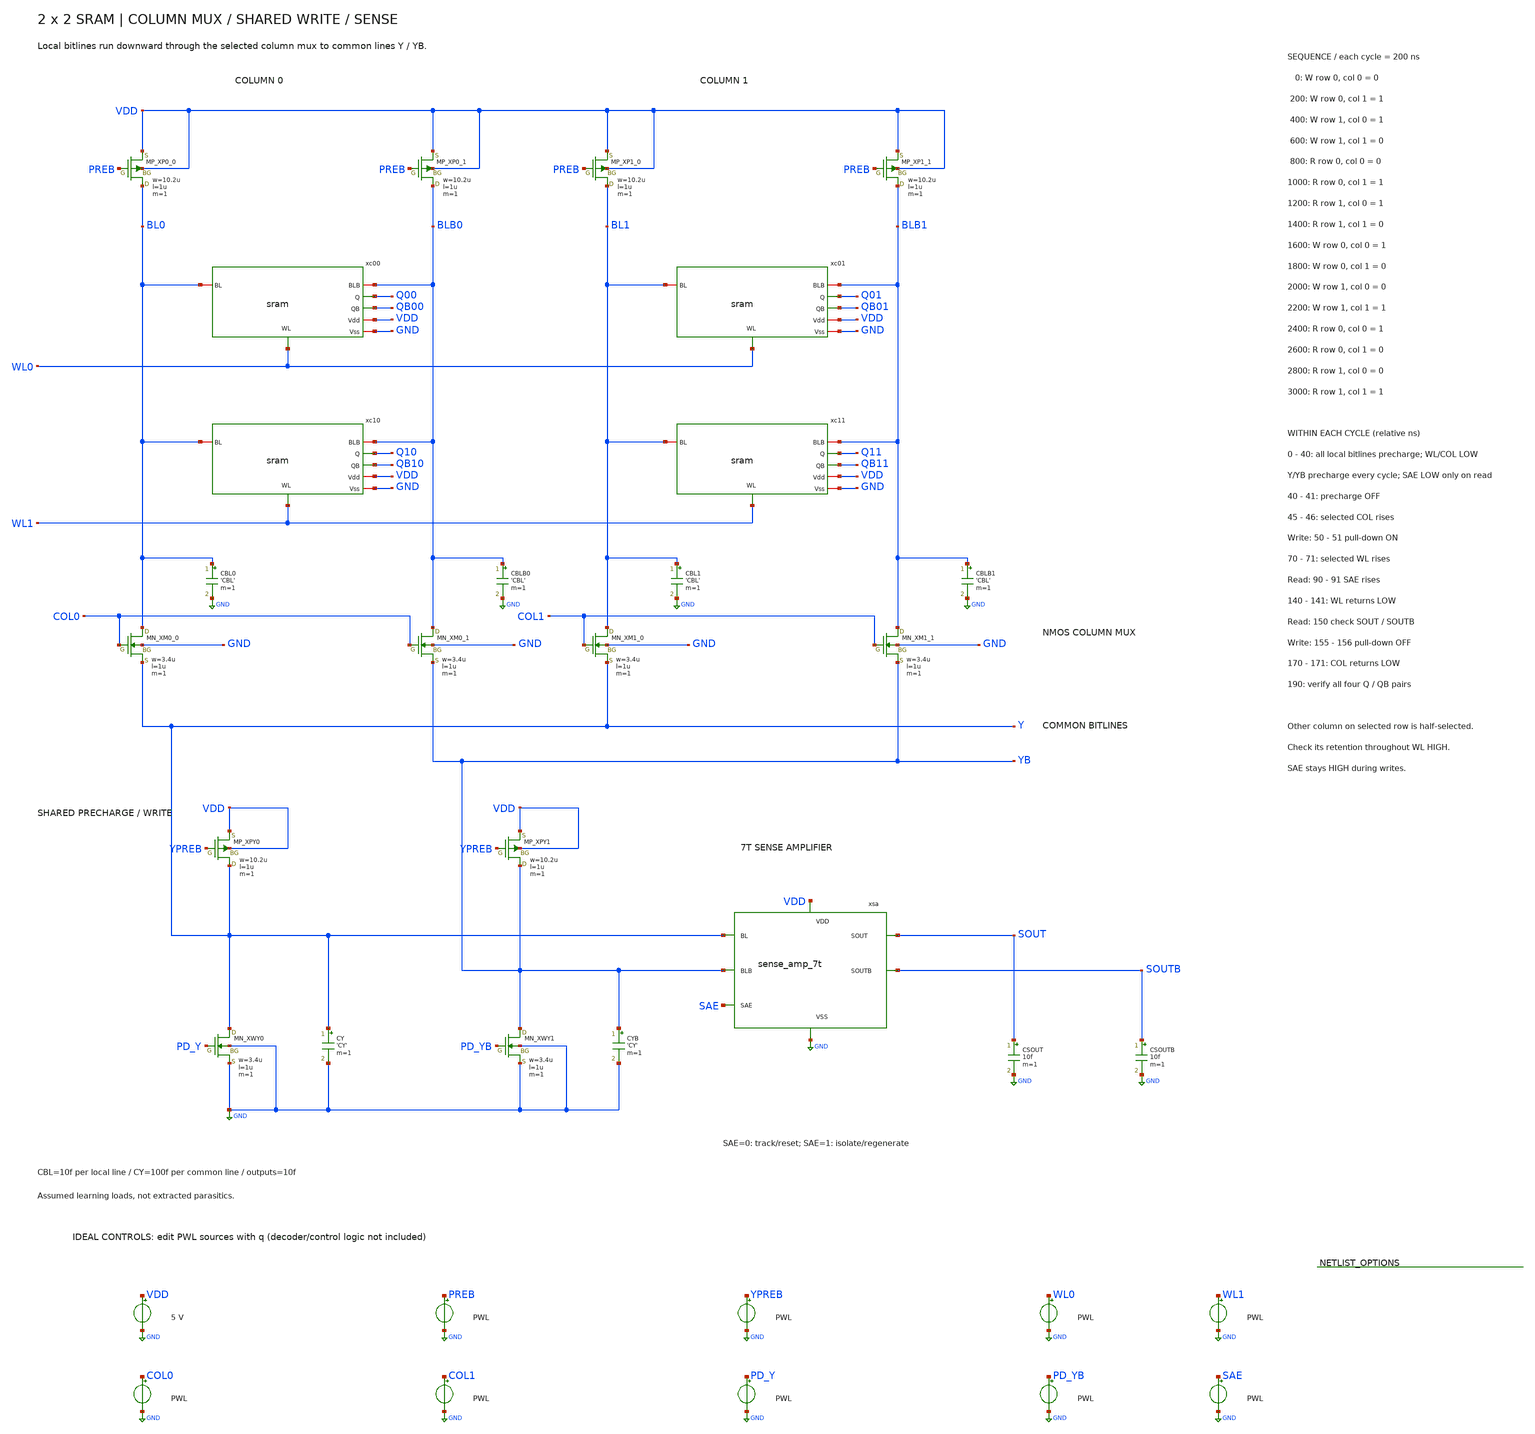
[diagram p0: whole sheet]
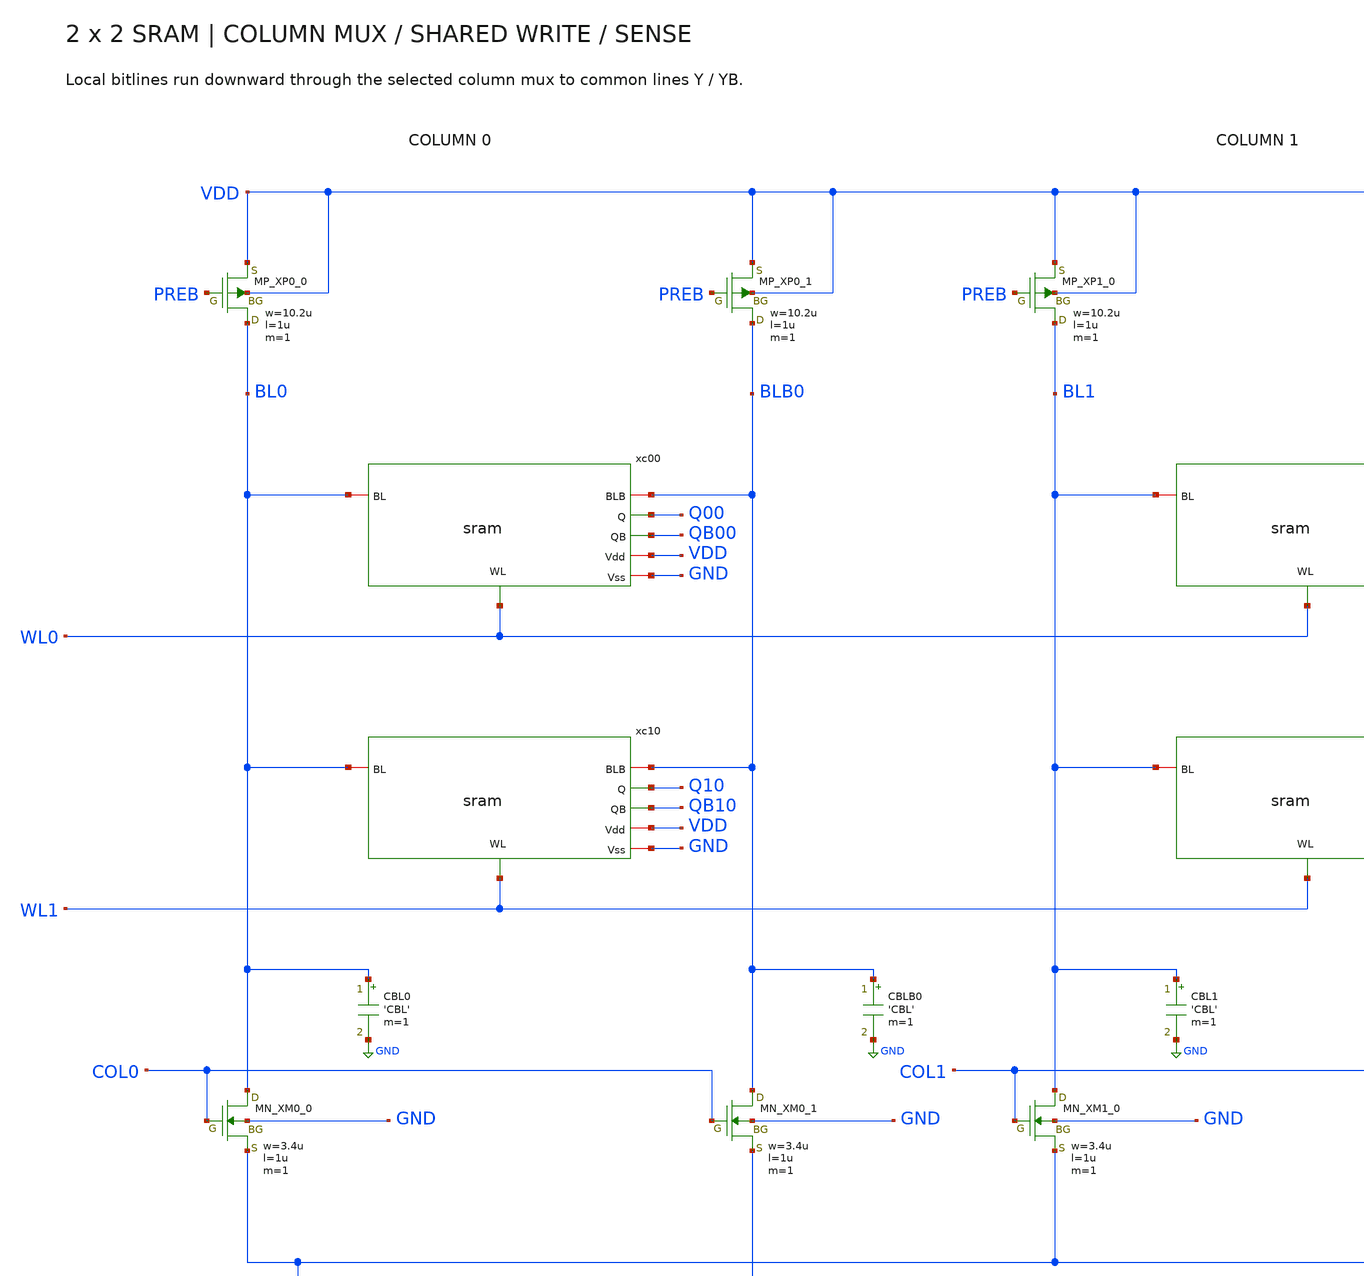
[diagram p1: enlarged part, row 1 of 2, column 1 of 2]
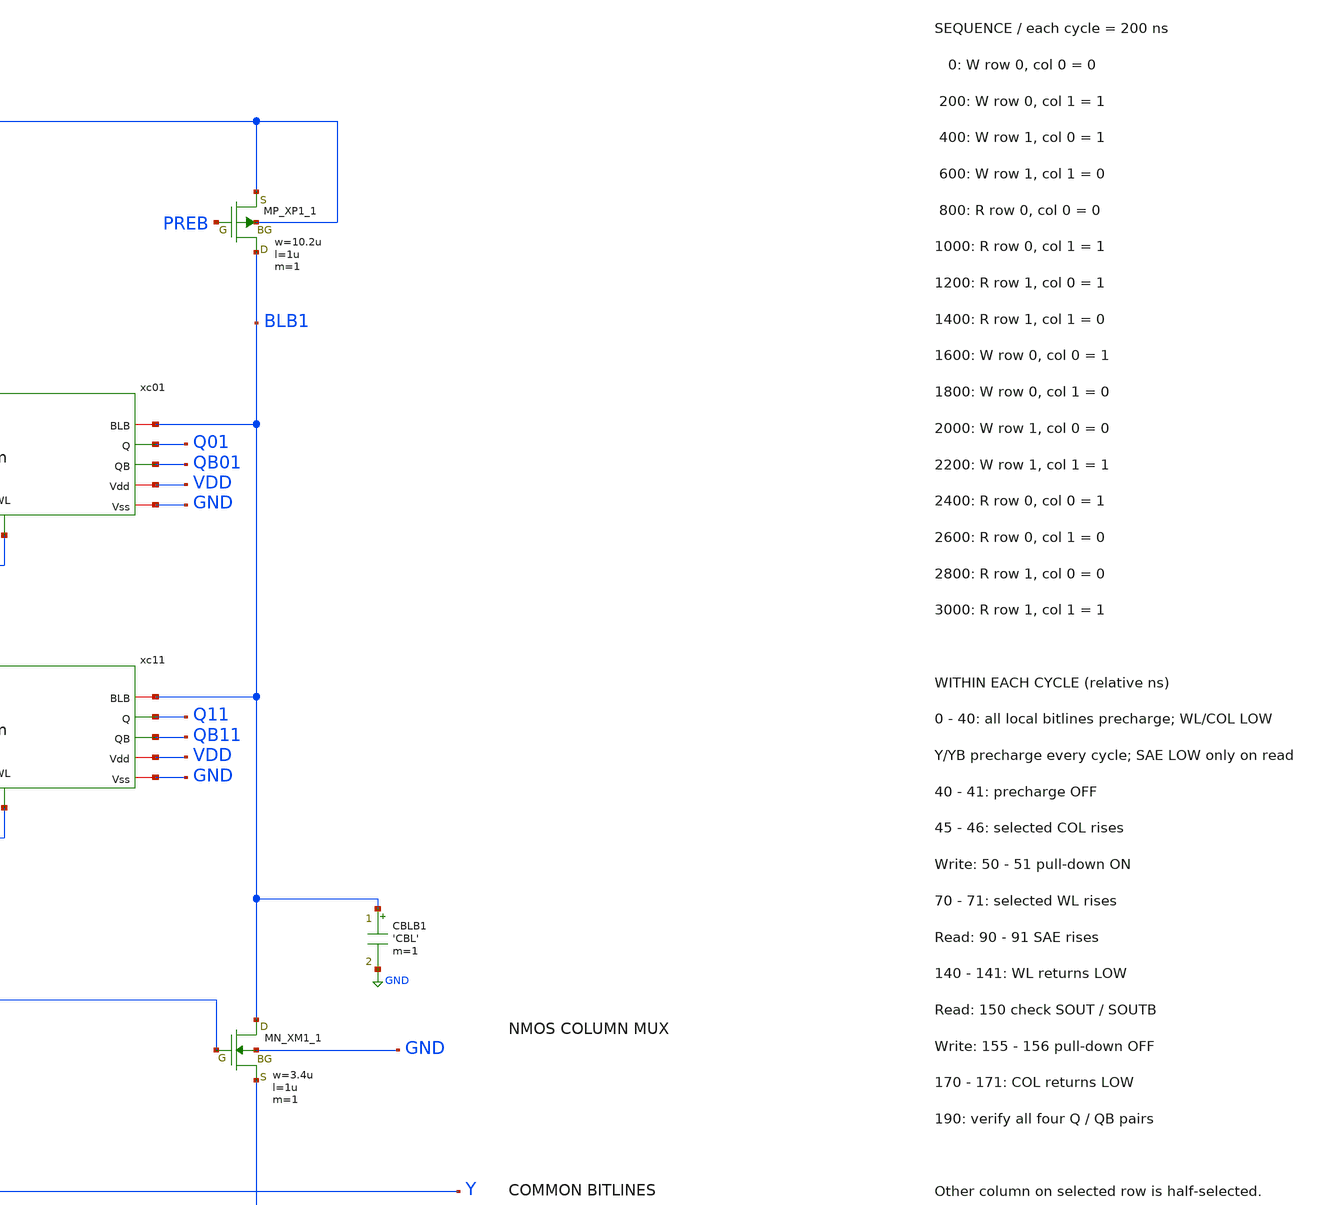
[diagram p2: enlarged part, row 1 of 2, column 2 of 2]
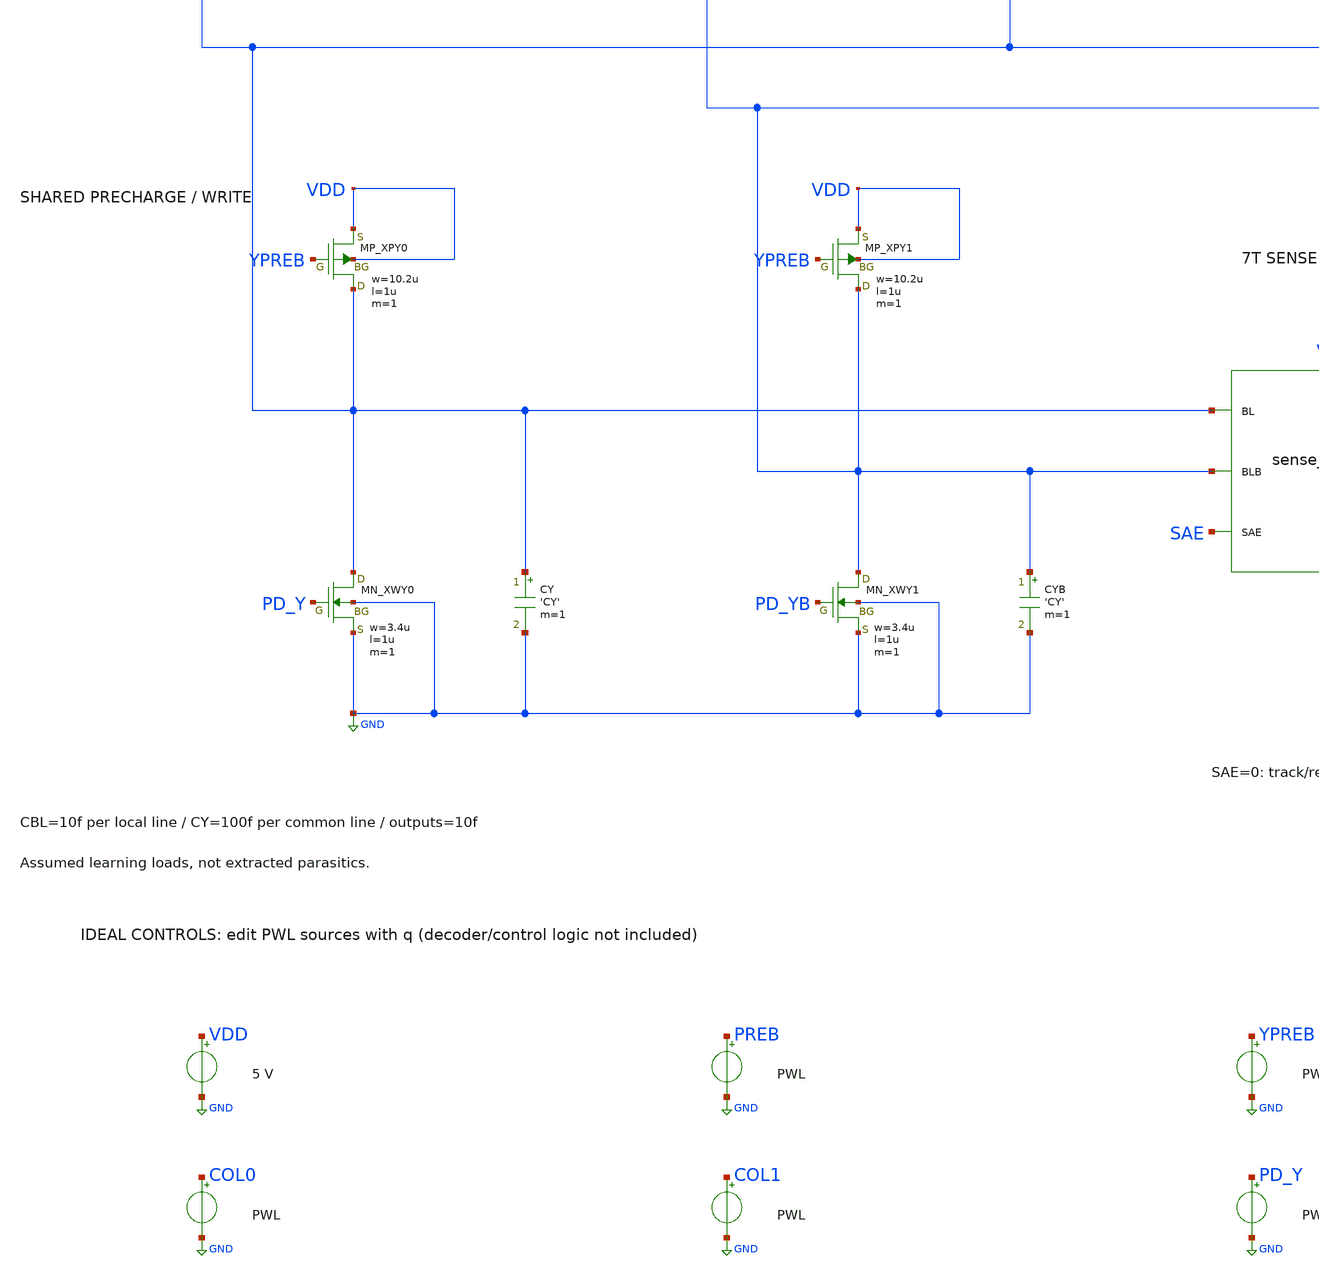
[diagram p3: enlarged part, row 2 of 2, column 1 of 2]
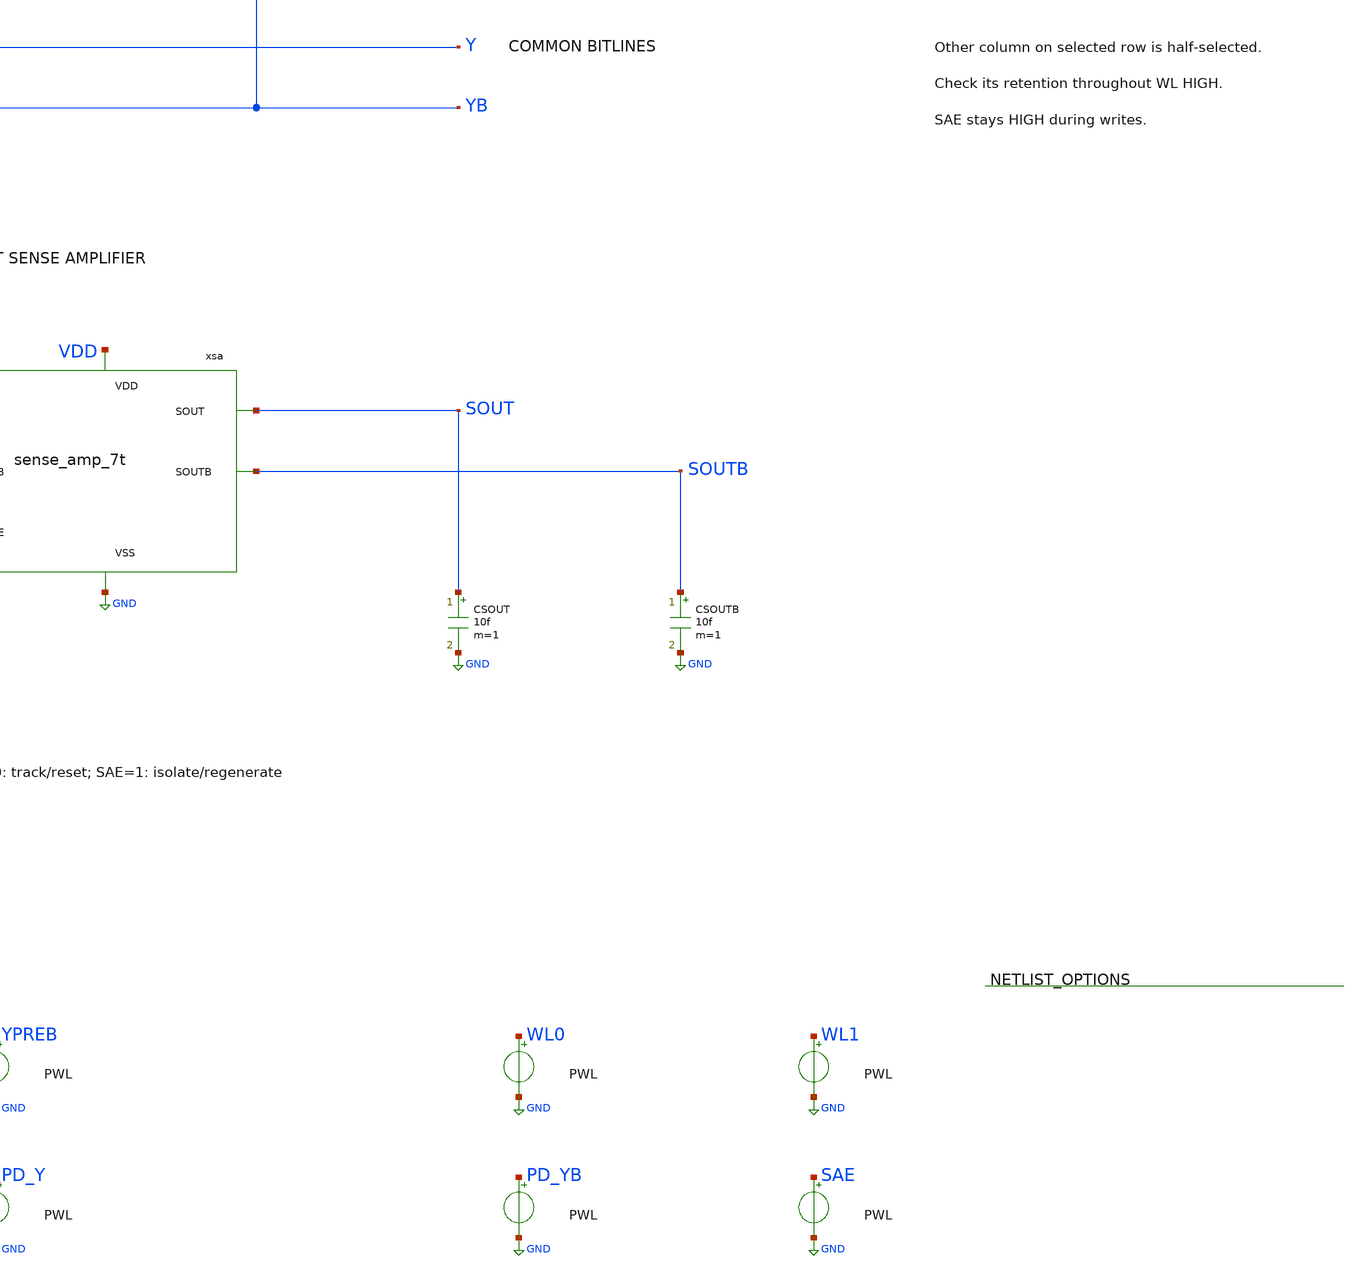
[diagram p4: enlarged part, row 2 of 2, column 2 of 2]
** sch_path: member_project/SRAM/PenguinEino/learning/schematics/sram_tb_array_mux.sch
**.subckt sram_tb_array_mux
XXP0_0 BL0 PREB VDD VDD PMOS w=10.2u l=1u nrd=0 nrs=0 m=1
CBL0 BL0 GND 'CBL' m=1
XXM0_0 BL0 COL0 Y GND NMOS w=3.4u l=1u nrd=0 nrs=0 m=1
XXP0_1 BLB0 PREB VDD VDD PMOS w=10.2u l=1u nrd=0 nrs=0 m=1
CBLB0 BLB0 GND 'CBL' m=1
XXM0_1 BLB0 COL0 YB GND NMOS w=3.4u l=1u nrd=0 nrs=0 m=1
xc00 WL0 VDD BLB0 Q00 QB00 BL0 GND sram
xc10 WL1 VDD BLB0 Q10 QB10 BL0 GND sram
XXP1_0 BL1 PREB VDD VDD PMOS w=10.2u l=1u nrd=0 nrs=0 m=1
CBL1 BL1 GND 'CBL' m=1
XXM1_0 BL1 COL1 Y GND NMOS w=3.4u l=1u nrd=0 nrs=0 m=1
XXP1_1 BLB1 PREB VDD VDD PMOS w=10.2u l=1u nrd=0 nrs=0 m=1
CBLB1 BLB1 GND 'CBL' m=1
XXM1_1 BLB1 COL1 YB GND NMOS w=3.4u l=1u nrd=0 nrs=0 m=1
xc01 WL0 VDD BLB1 Q01 QB01 BL1 GND sram
xc11 WL1 VDD BLB1 Q11 QB11 BL1 GND sram
XXPY0 Y YPREB VDD VDD PMOS w=10.2u l=1u nrd=0 nrs=0 m=1
XXWY0 Y PD_Y GND GND NMOS w=3.4u l=1u nrd=0 nrs=0 m=1
CY Y GND 'CY' m=1
XXPY1 YB YPREB VDD VDD PMOS w=10.2u l=1u nrd=0 nrs=0 m=1
XXWY1 YB PD_YB GND GND NMOS w=3.4u l=1u nrd=0 nrs=0 m=1
CYB YB GND 'CY' m=1
xsa Y YB SAE SOUT SOUTB VDD GND sense_amp_7t
CSOUT SOUT GND 10f m=1
CSOUTB SOUTB GND 10f m=1
VVDD VDD GND 5
VPREB PREB GND PWL(0n 0 40n 0 41n 5 200n 5 201n 0 240n 0 241n 5 400n 5 401n 0 440n 0 441n 5 600n 5
+ 601n 0 640n 0 641n 5 800n 5 801n 0 840n 0 841n 5 1000n 5 1001n 0 1040n 0 1041n 5 1200n 5 1201n 0 1240n 0
+ 1241n 5 1400n 5 1401n 0 1440n 0 1441n 5 1600n 5 1601n 0 1640n 0 1641n 5 1800n 5 1801n 0 1840n 0 1841n 5
+ 2000n 5 2001n 0 2040n 0 2041n 5 2200n 5 2201n 0 2240n 0 2241n 5 2400n 5 2401n 0 2440n 0 2441n 5 2600n 5
+ 2601n 0 2640n 0 2641n 5 2800n 5 2801n 0 2840n 0 2841n 5 3000n 5 3001n 0 3040n 0 3041n 5 3200n 5)
VYPREB YPREB GND PWL(0n 5 1n 5 2n 0 40n 0 41n 5 201n 5 202n 0 240n 0 241n 5 401n 5 402n 0 440n 0
+ 441n 5 601n 5 602n 0 640n 0 641n 5 801n 5 802n 0 840n 0 841n 5 1001n 5 1002n 0 1040n 0 1041n 5 1201n 5
+ 1202n 0 1240n 0 1241n 5 1401n 5 1402n 0 1440n 0 1441n 5 1601n 5 1602n 0 1640n 0 1641n 5 1801n 5 1802n 0
+ 1840n 0 1841n 5 2001n 5 2002n 0 2040n 0 2041n 5 2201n 5 2202n 0 2240n 0 2241n 5 2401n 5 2402n 0 2440n 0
+ 2441n 5 2601n 5 2602n 0 2640n 0 2641n 5 2801n 5 2802n 0 2840n 0 2841n 5 3001n 5 3002n 0 3040n 0 3041n 5
+ 3200n 5)
VWL0 WL0 GND PWL(0n 0 70n 0 71n 5 140n 5 141n 0 270n 0 271n 5 340n 5 341n 0 870n 0 871n 5 940n 5
+ 941n 0 1070n 0 1071n 5 1140n 5 1141n 0 1670n 0 1671n 5 1740n 5 1741n 0 1870n 0 1871n 5 1940n 5 1941n 0
+ 2470n 0 2471n 5 2540n 5 2541n 0 2670n 0 2671n 5 2740n 5 2741n 0 3200n 0)
VWL1 WL1 GND PWL(0n 0 470n 0 471n 5 540n 5 541n 0 670n 0 671n 5 740n 5 741n 0 1270n 0 1271n 5 1340n
+ 5 1341n 0 1470n 0 1471n 5 1540n 5 1541n 0 2070n 0 2071n 5 2140n 5 2141n 0 2270n 0 2271n 5 2340n 5
+ 2341n 0 2870n 0 2871n 5 2940n 5 2941n 0 3070n 0 3071n 5 3140n 5 3141n 0 3200n 0)
VCOL0 COL0 GND PWL(0n 0 45n 0 46n 5 170n 5 171n 0 445n 0 446n 5 570n 5 571n 0 845n 0 846n 5 970n 5
+ 971n 0 1245n 0 1246n 5 1370n 5 1371n 0 1645n 0 1646n 5 1770n 5 1771n 0 2045n 0 2046n 5 2170n 5 2171n 0
+ 2445n 0 2446n 5 2570n 5 2571n 0 2845n 0 2846n 5 2970n 5 2971n 0 3200n 0)
VCOL1 COL1 GND PWL(0n 0 245n 0 246n 5 370n 5 371n 0 645n 0 646n 5 770n 5 771n 0 1045n 0 1046n 5
+ 1170n 5 1171n 0 1445n 0 1446n 5 1570n 5 1571n 0 1845n 0 1846n 5 1970n 5 1971n 0 2245n 0 2246n 5 2370n 5
+ 2371n 0 2645n 0 2646n 5 2770n 5 2771n 0 3045n 0 3046n 5 3170n 5 3171n 0 3200n 0)
VPD_Y PD_Y GND PWL(0n 0 50n 0 51n 5 155n 5 156n 0 650n 0 651n 5 755n 5 756n 0 1850n 0 1851n 5 1955n
+ 5 1956n 0 2050n 0 2051n 5 2155n 5 2156n 0 3200n 0)
VPD_YB PD_YB GND PWL(0n 0 250n 0 251n 5 355n 5 356n 0 450n 0 451n 5 555n 5 556n 0 1650n 0 1651n 5
+ 1755n 5 1756n 0 2250n 0 2251n 5 2355n 5 2356n 0 3200n 0)
VSAE SAE GND PWL(0n 5 801n 5 802n 0 890n 0 891n 5 1001n 5 1002n 0 1090n 0 1091n 5 1201n 5 1202n 0
+ 1290n 0 1291n 5 1401n 5 1402n 0 1490n 0 1491n 5 2401n 5 2402n 0 2490n 0 2491n 5 2601n 5 2602n 0 2690n 0
+ 2691n 5 2801n 5 2802n 0 2890n 0 2891n 5 3001n 5 3002n 0 3090n 0 3091n 5 3200n 5)
**** begin user architecture code
 .include $::LIB/ip62_models

.param CBL=10f CY=100f
.ic v(Q00)=0 v(QB00)=5 v(Q01)=0 v(QB01)=5 v(Q10)=0 v(QB10)=5 v(Q11)=0 v(QB11)=5
.control
save all
tran 0.1n 3200n
let failures = 0
let ydiff = v(Y)-v(YB)
meas tran h_0_Q00 find v(Q00) at=190n
if h_0_Q00 > 0.5
 let failures = failures + 1
end
meas tran h_0_QB00 find v(QB00) at=190n
if h_0_QB00 < 4.5
 let failures = failures + 1
end
meas tran h_0_Q01 find v(Q01) at=190n
if h_0_Q01 > 0.5
 let failures = failures + 1
end
meas tran keep_0_Q01 max v(Q01) from=69n to=142n
if keep_0_Q01 > 2.5
 let failures = failures + 1
end
meas tran h_0_QB01 find v(QB01) at=190n
if h_0_QB01 < 4.5
 let failures = failures + 1
end
meas tran keep_0_QB01 min v(QB01) from=69n to=142n
if keep_0_QB01 < 2.5
 let failures = failures + 1
end
meas tran h_0_Q10 find v(Q10) at=190n
if h_0_Q10 > 0.5
 let failures = failures + 1
end
meas tran keep_0_Q10 max v(Q10) from=69n to=142n
if keep_0_Q10 > 2.5
 let failures = failures + 1
end
meas tran h_0_QB10 find v(QB10) at=190n
if h_0_QB10 < 4.5
 let failures = failures + 1
end
meas tran keep_0_QB10 min v(QB10) from=69n to=142n
if keep_0_QB10 < 2.5
 let failures = failures + 1
end
meas tran h_0_Q11 find v(Q11) at=190n
if h_0_Q11 > 0.5
 let failures = failures + 1
end
meas tran keep_0_Q11 max v(Q11) from=69n to=142n
if keep_0_Q11 > 2.5
 let failures = failures + 1
end
meas tran h_0_QB11 find v(QB11) at=190n
if h_0_QB11 < 4.5
 let failures = failures + 1
end
meas tran keep_0_QB11 min v(QB11) from=69n to=142n
if keep_0_QB11 < 2.5
 let failures = failures + 1
end
meas tran h_1_Q00 find v(Q00) at=390n
if h_1_Q00 > 0.5
 let failures = failures + 1
end
meas tran keep_1_Q00 max v(Q00) from=269n to=342n
if keep_1_Q00 > 2.5
 let failures = failures + 1
end
meas tran h_1_QB00 find v(QB00) at=390n
if h_1_QB00 < 4.5
 let failures = failures + 1
end
meas tran keep_1_QB00 min v(QB00) from=269n to=342n
if keep_1_QB00 < 2.5
 let failures = failures + 1
end
meas tran h_1_Q01 find v(Q01) at=390n
if h_1_Q01 < 4.5
 let failures = failures + 1
end
meas tran h_1_QB01 find v(QB01) at=390n
if h_1_QB01 > 0.5
 let failures = failures + 1
end
meas tran h_1_Q10 find v(Q10) at=390n
if h_1_Q10 > 0.5
 let failures = failures + 1
end
meas tran keep_1_Q10 max v(Q10) from=269n to=342n
if keep_1_Q10 > 2.5
 let failures = failures + 1
end
meas tran h_1_QB10 find v(QB10) at=390n
if h_1_QB10 < 4.5
 let failures = failures + 1
end
meas tran keep_1_QB10 min v(QB10) from=269n to=342n
if keep_1_QB10 < 2.5
 let failures = failures + 1
end
meas tran h_1_Q11 find v(Q11) at=390n
if h_1_Q11 > 0.5
 let failures = failures + 1
end
meas tran keep_1_Q11 max v(Q11) from=269n to=342n
if keep_1_Q11 > 2.5
 let failures = failures + 1
end
meas tran h_1_QB11 find v(QB11) at=390n
if h_1_QB11 < 4.5
 let failures = failures + 1
end
meas tran keep_1_QB11 min v(QB11) from=269n to=342n
if keep_1_QB11 < 2.5
 let failures = failures + 1
end
meas tran h_2_Q00 find v(Q00) at=590n
if h_2_Q00 > 0.5
 let failures = failures + 1
end
meas tran keep_2_Q00 max v(Q00) from=469n to=542n
if keep_2_Q00 > 2.5
 let failures = failures + 1
end
meas tran h_2_QB00 find v(QB00) at=590n
if h_2_QB00 < 4.5
 let failures = failures + 1
end
meas tran keep_2_QB00 min v(QB00) from=469n to=542n
if keep_2_QB00 < 2.5
 let failures = failures + 1
end
meas tran h_2_Q01 find v(Q01) at=590n
if h_2_Q01 < 4.5
 let failures = failures + 1
end
meas tran keep_2_Q01 min v(Q01) from=469n to=542n
if keep_2_Q01 < 2.5
 let failures = failures + 1
end
meas tran h_2_QB01 find v(QB01) at=590n
if h_2_QB01 > 0.5
 let failures = failures + 1
end
meas tran keep_2_QB01 max v(QB01) from=469n to=542n
if keep_2_QB01 > 2.5
 let failures = failures + 1
end
meas tran h_2_Q10 find v(Q10) at=590n
if h_2_Q10 < 4.5
 let failures = failures + 1
end
meas tran h_2_QB10 find v(QB10) at=590n
if h_2_QB10 > 0.5
 let failures = failures + 1
end
meas tran h_2_Q11 find v(Q11) at=590n
if h_2_Q11 > 0.5
 let failures = failures + 1
end
meas tran keep_2_Q11 max v(Q11) from=469n to=542n
if keep_2_Q11 > 2.5
 let failures = failures + 1
end
meas tran h_2_QB11 find v(QB11) at=590n
if h_2_QB11 < 4.5
 let failures = failures + 1
end
meas tran keep_2_QB11 min v(QB11) from=469n to=542n
if keep_2_QB11 < 2.5
 let failures = failures + 1
end
meas tran h_3_Q00 find v(Q00) at=790n
if h_3_Q00 > 0.5
 let failures = failures + 1
end
meas tran keep_3_Q00 max v(Q00) from=669n to=742n
if keep_3_Q00 > 2.5
 let failures = failures + 1
end
meas tran h_3_QB00 find v(QB00) at=790n
if h_3_QB00 < 4.5
 let failures = failures + 1
end
meas tran keep_3_QB00 min v(QB00) from=669n to=742n
if keep_3_QB00 < 2.5
 let failures = failures + 1
end
meas tran h_3_Q01 find v(Q01) at=790n
if h_3_Q01 < 4.5
 let failures = failures + 1
end
meas tran keep_3_Q01 min v(Q01) from=669n to=742n
if keep_3_Q01 < 2.5
 let failures = failures + 1
end
meas tran h_3_QB01 find v(QB01) at=790n
if h_3_QB01 > 0.5
 let failures = failures + 1
end
meas tran keep_3_QB01 max v(QB01) from=669n to=742n
if keep_3_QB01 > 2.5
 let failures = failures + 1
end
meas tran h_3_Q10 find v(Q10) at=790n
if h_3_Q10 < 4.5
 let failures = failures + 1
end
meas tran keep_3_Q10 min v(Q10) from=669n to=742n
if keep_3_Q10 < 2.5
 let failures = failures + 1
end
meas tran h_3_QB10 find v(QB10) at=790n
if h_3_QB10 > 0.5
 let failures = failures + 1
end
meas tran keep_3_QB10 max v(QB10) from=669n to=742n
if keep_3_QB10 > 2.5
 let failures = failures + 1
end
meas tran h_3_Q11 find v(Q11) at=790n
if h_3_Q11 > 0.5
 let failures = failures + 1
end
meas tran h_3_QB11 find v(QB11) at=790n
if h_3_QB11 < 4.5
 let failures = failures + 1
end
meas tran h_4_Q00 find v(Q00) at=990n
if h_4_Q00 > 0.5
 let failures = failures + 1
end
meas tran keep_4_Q00 max v(Q00) from=869n to=942n
if keep_4_Q00 > 2.5
 let failures = failures + 1
end
meas tran h_4_QB00 find v(QB00) at=990n
if h_4_QB00 < 4.5
 let failures = failures + 1
end
meas tran keep_4_QB00 min v(QB00) from=869n to=942n
if keep_4_QB00 < 2.5
 let failures = failures + 1
end
meas tran h_4_Q01 find v(Q01) at=990n
if h_4_Q01 < 4.5
 let failures = failures + 1
end
meas tran keep_4_Q01 min v(Q01) from=869n to=942n
if keep_4_Q01 < 2.5
 let failures = failures + 1
end
meas tran h_4_QB01 find v(QB01) at=990n
if h_4_QB01 > 0.5
 let failures = failures + 1
end
meas tran keep_4_QB01 max v(QB01) from=869n to=942n
if keep_4_QB01 > 2.5
 let failures = failures + 1
end
meas tran h_4_Q10 find v(Q10) at=990n
if h_4_Q10 < 4.5
 let failures = failures + 1
end
meas tran keep_4_Q10 min v(Q10) from=869n to=942n
if keep_4_Q10 < 2.5
 let failures = failures + 1
end
meas tran h_4_QB10 find v(QB10) at=990n
if h_4_QB10 > 0.5
 let failures = failures + 1
end
meas tran keep_4_QB10 max v(QB10) from=869n to=942n
if keep_4_QB10 > 2.5
 let failures = failures + 1
end
meas tran h_4_Q11 find v(Q11) at=990n
if h_4_Q11 > 0.5
 let failures = failures + 1
end
meas tran keep_4_Q11 max v(Q11) from=869n to=942n
if keep_4_Q11 > 2.5
 let failures = failures + 1
end
meas tran h_4_QB11 find v(QB11) at=990n
if h_4_QB11 < 4.5
 let failures = failures + 1
end
meas tran keep_4_QB11 min v(QB11) from=869n to=942n
if keep_4_QB11 < 2.5
 let failures = failures + 1
end
meas tran reset_4_SOUT find v(SOUT) at=839n
if reset_4_SOUT < 4.5
 let failures = failures + 1
end
meas tran read_4_SOUT find v(SOUT) at=950n
if read_4_SOUT > 0.5
 let failures = failures + 1
end
meas tran reset_4_SOUTB find v(SOUTB) at=839n
if reset_4_SOUTB < 4.5
 let failures = failures + 1
end
meas tran read_4_SOUTB find v(SOUTB) at=950n
if read_4_SOUTB < 4.5
 let failures = failures + 1
end
meas tran diff_4 find ydiff at=890n
meas tran h_5_Q00 find v(Q00) at=1190n
if h_5_Q00 > 0.5
 let failures = failures + 1
end
meas tran keep_5_Q00 max v(Q00) from=1069n to=1142n
if keep_5_Q00 > 2.5
 let failures = failures + 1
end
meas tran h_5_QB00 find v(QB00) at=1190n
if h_5_QB00 < 4.5
 let failures = failures + 1
end
meas tran keep_5_QB00 min v(QB00) from=1069n to=1142n
if keep_5_QB00 < 2.5
 let failures = failures + 1
end
meas tran h_5_Q01 find v(Q01) at=1190n
if h_5_Q01 < 4.5
 let failures = failures + 1
end
meas tran keep_5_Q01 min v(Q01) from=1069n to=1142n
if keep_5_Q01 < 2.5
 let failures = failures + 1
end
meas tran h_5_QB01 find v(QB01) at=1190n
if h_5_QB01 > 0.5
 let failures = failures + 1
end
meas tran keep_5_QB01 max v(QB01) from=1069n to=1142n
if keep_5_QB01 > 2.5
 let failures = failures + 1
end
meas tran h_5_Q10 find v(Q10) at=1190n
if h_5_Q10 < 4.5
 let failures = failures + 1
end
meas tran keep_5_Q10 min v(Q10) from=1069n to=1142n
if keep_5_Q10 < 2.5
 let failures = failures + 1
end
meas tran h_5_QB10 find v(QB10) at=1190n
if h_5_QB10 > 0.5
 let failures = failures + 1
end
meas tran keep_5_QB10 max v(QB10) from=1069n to=1142n
if keep_5_QB10 > 2.5
 let failures = failures + 1
end
meas tran h_5_Q11 find v(Q11) at=1190n
if h_5_Q11 > 0.5
 let failures = failures + 1
end
meas tran keep_5_Q11 max v(Q11) from=1069n to=1142n
if keep_5_Q11 > 2.5
 let failures = failures + 1
end
meas tran h_5_QB11 find v(QB11) at=1190n
if h_5_QB11 < 4.5
 let failures = failures + 1
end
meas tran keep_5_QB11 min v(QB11) from=1069n to=1142n
if keep_5_QB11 < 2.5
 let failures = failures + 1
end
meas tran reset_5_SOUT find v(SOUT) at=1039n
if reset_5_SOUT < 4.5
 let failures = failures + 1
end
meas tran read_5_SOUT find v(SOUT) at=1150n
if read_5_SOUT < 4.5
 let failures = failures + 1
end
meas tran reset_5_SOUTB find v(SOUTB) at=1039n
if reset_5_SOUTB < 4.5
 let failures = failures + 1
end
meas tran read_5_SOUTB find v(SOUTB) at=1150n
if read_5_SOUTB > 0.5
 let failures = failures + 1
end
meas tran diff_5 find ydiff at=1090n
meas tran h_6_Q00 find v(Q00) at=1390n
if h_6_Q00 > 0.5
 let failures = failures + 1
end
meas tran keep_6_Q00 max v(Q00) from=1269n to=1342n
if keep_6_Q00 > 2.5
 let failures = failures + 1
end
meas tran h_6_QB00 find v(QB00) at=1390n
if h_6_QB00 < 4.5
 let failures = failures + 1
end
meas tran keep_6_QB00 min v(QB00) from=1269n to=1342n
if keep_6_QB00 < 2.5
 let failures = failures + 1
end
meas tran h_6_Q01 find v(Q01) at=1390n
if h_6_Q01 < 4.5
 let failures = failures + 1
end
meas tran keep_6_Q01 min v(Q01) from=1269n to=1342n
if keep_6_Q01 < 2.5
 let failures = failures + 1
end
meas tran h_6_QB01 find v(QB01) at=1390n
if h_6_QB01 > 0.5
 let failures = failures + 1
end
meas tran keep_6_QB01 max v(QB01) from=1269n to=1342n
if keep_6_QB01 > 2.5
 let failures = failures + 1
end
meas tran h_6_Q10 find v(Q10) at=1390n
if h_6_Q10 < 4.5
 let failures = failures + 1
end
meas tran keep_6_Q10 min v(Q10) from=1269n to=1342n
if keep_6_Q10 < 2.5
 let failures = failures + 1
end
meas tran h_6_QB10 find v(QB10) at=1390n
if h_6_QB10 > 0.5
 let failures = failures + 1
end
meas tran keep_6_QB10 max v(QB10) from=1269n to=1342n
if keep_6_QB10 > 2.5
 let failures = failures + 1
end
meas tran h_6_Q11 find v(Q11) at=1390n
if h_6_Q11 > 0.5
 let failures = failures + 1
end
meas tran keep_6_Q11 max v(Q11) from=1269n to=1342n
if keep_6_Q11 > 2.5
 let failures = failures + 1
end
meas tran h_6_QB11 find v(QB11) at=1390n
if h_6_QB11 < 4.5
 let failures = failures + 1
end
meas tran keep_6_QB11 min v(QB11) from=1269n to=1342n
if keep_6_QB11 < 2.5
 let failures = failures + 1
end
meas tran reset_6_SOUT find v(SOUT) at=1239n
if reset_6_SOUT < 4.5
 let failures = failures + 1
end
meas tran read_6_SOUT find v(SOUT) at=1350n
if read_6_SOUT < 4.5
 let failures = failures + 1
end
meas tran reset_6_SOUTB find v(SOUTB) at=1239n
if reset_6_SOUTB < 4.5
 let failures = failures + 1
end
meas tran read_6_SOUTB find v(SOUTB) at=1350n
if read_6_SOUTB > 0.5
 let failures = failures + 1
end
meas tran diff_6 find ydiff at=1290n
meas tran h_7_Q00 find v(Q00) at=1590n
if h_7_Q00 > 0.5
 let failures = failures + 1
end
meas tran keep_7_Q00 max v(Q00) from=1469n to=1542n
if keep_7_Q00 > 2.5
 let failures = failures + 1
end
meas tran h_7_QB00 find v(QB00) at=1590n
if h_7_QB00 < 4.5
 let failures = failures + 1
end
meas tran keep_7_QB00 min v(QB00) from=1469n to=1542n
if keep_7_QB00 < 2.5
 let failures = failures + 1
end
meas tran h_7_Q01 find v(Q01) at=1590n
if h_7_Q01 < 4.5
 let failures = failures + 1
end
meas tran keep_7_Q01 min v(Q01) from=1469n to=1542n
if keep_7_Q01 < 2.5
 let failures = failures + 1
end
meas tran h_7_QB01 find v(QB01) at=1590n
if h_7_QB01 > 0.5
 let failures = failures + 1
end
meas tran keep_7_QB01 max v(QB01) from=1469n to=1542n
if keep_7_QB01 > 2.5
 let failures = failures + 1
end
meas tran h_7_Q10 find v(Q10) at=1590n
if h_7_Q10 < 4.5
 let failures = failures + 1
end
meas tran keep_7_Q10 min v(Q10) from=1469n to=1542n
if keep_7_Q10 < 2.5
 let failures = failures + 1
end
meas tran h_7_QB10 find v(QB10) at=1590n
if h_7_QB10 > 0.5
 let failures = failures + 1
end
meas tran keep_7_QB10 max v(QB10) from=1469n to=1542n
if keep_7_QB10 > 2.5
 let failures = failures + 1
end
meas tran h_7_Q11 find v(Q11) at=1590n
if h_7_Q11 > 0.5
 let failures = failures + 1
end
meas tran keep_7_Q11 max v(Q11) from=1469n to=1542n
if keep_7_Q11 > 2.5
 let failures = failures + 1
end
meas tran h_7_QB11 find v(QB11) at=1590n
if h_7_QB11 < 4.5
 let failures = failures + 1
end
meas tran keep_7_QB11 min v(QB11) from=1469n to=1542n
if keep_7_QB11 < 2.5
 let failures = failures + 1
end
meas tran reset_7_SOUT find v(SOUT) at=1439n
if reset_7_SOUT < 4.5
 let failures = failures + 1
end
meas tran read_7_SOUT find v(SOUT) at=1550n
if read_7_SOUT > 0.5
 let failures = failures + 1
end
meas tran reset_7_SOUTB find v(SOUTB) at=1439n
if reset_7_SOUTB < 4.5
 let failures = failures + 1
end
meas tran read_7_SOUTB find v(SOUTB) at=1550n
if read_7_SOUTB < 4.5
 let failures = failures + 1
end
meas tran diff_7 find ydiff at=1490n
meas tran h_8_Q00 find v(Q00) at=1790n
if h_8_Q00 < 4.5
 let failures = failures + 1
end
meas tran h_8_QB00 find v(QB00) at=1790n
if h_8_QB00 > 0.5
 let failures = failures + 1
end
meas tran h_8_Q01 find v(Q01) at=1790n
if h_8_Q01 < 4.5
 let failures = failures + 1
end
meas tran keep_8_Q01 min v(Q01) from=1669n to=1742n
if keep_8_Q01 < 2.5
 let failures = failures + 1
end
meas tran h_8_QB01 find v(QB01) at=1790n
if h_8_QB01 > 0.5
 let failures = failures + 1
end
meas tran keep_8_QB01 max v(QB01) from=1669n to=1742n
if keep_8_QB01 > 2.5
 let failures = failures + 1
end
meas tran h_8_Q10 find v(Q10) at=1790n
if h_8_Q10 < 4.5
 let failures = failures + 1
end
meas tran keep_8_Q10 min v(Q10) from=1669n to=1742n
if keep_8_Q10 < 2.5
 let failures = failures + 1
end
meas tran h_8_QB10 find v(QB10) at=1790n
if h_8_QB10 > 0.5
 let failures = failures + 1
end
meas tran keep_8_QB10 max v(QB10) from=1669n to=1742n
if keep_8_QB10 > 2.5
 let failures = failures + 1
end
meas tran h_8_Q11 find v(Q11) at=1790n
if h_8_Q11 > 0.5
 let failures = failures + 1
end
meas tran keep_8_Q11 max v(Q11) from=1669n to=1742n
if keep_8_Q11 > 2.5
 let failures = failures + 1
end
meas tran h_8_QB11 find v(QB11) at=1790n
if h_8_QB11 < 4.5
 let failures = failures + 1
end
meas tran keep_8_QB11 min v(QB11) from=1669n to=1742n
if keep_8_QB11 < 2.5
 let failures = failures + 1
end
meas tran h_9_Q00 find v(Q00) at=1990n
if h_9_Q00 < 4.5
 let failures = failures + 1
end
meas tran keep_9_Q00 min v(Q00) from=1869n to=1942n
if keep_9_Q00 < 2.5
 let failures = failures + 1
end
meas tran h_9_QB00 find v(QB00) at=1990n
if h_9_QB00 > 0.5
 let failures = failures + 1
end
meas tran keep_9_QB00 max v(QB00) from=1869n to=1942n
if keep_9_QB00 > 2.5
 let failures = failures + 1
end
meas tran h_9_Q01 find v(Q01) at=1990n
if h_9_Q01 > 0.5
 let failures = failures + 1
end
meas tran h_9_QB01 find v(QB01) at=1990n
if h_9_QB01 < 4.5
 let failures = failures + 1
end
meas tran h_9_Q10 find v(Q10) at=1990n
if h_9_Q10 < 4.5
 let failures = failures + 1
end
meas tran keep_9_Q10 min v(Q10) from=1869n to=1942n
if keep_9_Q10 < 2.5
 let failures = failures + 1
end
meas tran h_9_QB10 find v(QB10) at=1990n
if h_9_QB10 > 0.5
 let failures = failures + 1
end
meas tran keep_9_QB10 max v(QB10) from=1869n to=1942n
if keep_9_QB10 > 2.5
 let failures = failures + 1
end
meas tran h_9_Q11 find v(Q11) at=1990n
if h_9_Q11 > 0.5
 let failures = failures + 1
end
meas tran keep_9_Q11 max v(Q11) from=1869n to=1942n
if keep_9_Q11 > 2.5
 let failures = failures + 1
end
meas tran h_9_QB11 find v(QB11) at=1990n
if h_9_QB11 < 4.5
 let failures = failures + 1
end
meas tran keep_9_QB11 min v(QB11) from=1869n to=1942n
if keep_9_QB11 < 2.5
 let failures = failures + 1
end
meas tran h_10_Q00 find v(Q00) at=2190n
if h_10_Q00 < 4.5
 let failures = failures + 1
end
meas tran keep_10_Q00 min v(Q00) from=2069n to=2142n
if keep_10_Q00 < 2.5
 let failures = failures + 1
end
meas tran h_10_QB00 find v(QB00) at=2190n
if h_10_QB00 > 0.5
 let failures = failures + 1
end
meas tran keep_10_QB00 max v(QB00) from=2069n to=2142n
if keep_10_QB00 > 2.5
 let failures = failures + 1
end
meas tran h_10_Q01 find v(Q01) at=2190n
if h_10_Q01 > 0.5
 let failures = failures + 1
end
meas tran keep_10_Q01 max v(Q01) from=2069n to=2142n
if keep_10_Q01 > 2.5
 let failures = failures + 1
end
meas tran h_10_QB01 find v(QB01) at=2190n
if h_10_QB01 < 4.5
 let failures = failures + 1
end
meas tran keep_10_QB01 min v(QB01) from=2069n to=2142n
if keep_10_QB01 < 2.5
 let failures = failures + 1
end
meas tran h_10_Q10 find v(Q10) at=2190n
if h_10_Q10 > 0.5
 let failures = failures + 1
end
meas tran h_10_QB10 find v(QB10) at=2190n
if h_10_QB10 < 4.5
 let failures = failures + 1
end
meas tran h_10_Q11 find v(Q11) at=2190n
if h_10_Q11 > 0.5
 let failures = failures + 1
end
meas tran keep_10_Q11 max v(Q11) from=2069n to=2142n
if keep_10_Q11 > 2.5
 let failures = failures + 1
end
meas tran h_10_QB11 find v(QB11) at=2190n
if h_10_QB11 < 4.5
 let failures = failures + 1
end
meas tran keep_10_QB11 min v(QB11) from=2069n to=2142n
if keep_10_QB11 < 2.5
 let failures = failures + 1
end
meas tran h_11_Q00 find v(Q00) at=2390n
if h_11_Q00 < 4.5
 let failures = failures + 1
end
meas tran keep_11_Q00 min v(Q00) from=2269n to=2342n
if keep_11_Q00 < 2.5
 let failures = failures + 1
end
meas tran h_11_QB00 find v(QB00) at=2390n
if h_11_QB00 > 0.5
 let failures = failures + 1
end
meas tran keep_11_QB00 max v(QB00) from=2269n to=2342n
if keep_11_QB00 > 2.5
 let failures = failures + 1
end
meas tran h_11_Q01 find v(Q01) at=2390n
if h_11_Q01 > 0.5
 let failures = failures + 1
end
meas tran keep_11_Q01 max v(Q01) from=2269n to=2342n
if keep_11_Q01 > 2.5
 let failures = failures + 1
end
meas tran h_11_QB01 find v(QB01) at=2390n
if h_11_QB01 < 4.5
 let failures = failures + 1
end
meas tran keep_11_QB01 min v(QB01) from=2269n to=2342n
if keep_11_QB01 < 2.5
 let failures = failures + 1
end
meas tran h_11_Q10 find v(Q10) at=2390n
if h_11_Q10 > 0.5
 let failures = failures + 1
end
meas tran keep_11_Q10 max v(Q10) from=2269n to=2342n
if keep_11_Q10 > 2.5
 let failures = failures + 1
end
meas tran h_11_QB10 find v(QB10) at=2390n
if h_11_QB10 < 4.5
 let failures = failures + 1
end
meas tran keep_11_QB10 min v(QB10) from=2269n to=2342n
if keep_11_QB10 < 2.5
 let failures = failures + 1
end
meas tran h_11_Q11 find v(Q11) at=2390n
if h_11_Q11 < 4.5
 let failures = failures + 1
end
meas tran h_11_QB11 find v(QB11) at=2390n
if h_11_QB11 > 0.5
 let failures = failures + 1
end
meas tran h_12_Q00 find v(Q00) at=2590n
if h_12_Q00 < 4.5
 let failures = failures + 1
end
meas tran keep_12_Q00 min v(Q00) from=2469n to=2542n
if keep_12_Q00 < 2.5
 let failures = failures + 1
end
meas tran h_12_QB00 find v(QB00) at=2590n
if h_12_QB00 > 0.5
 let failures = failures + 1
end
meas tran keep_12_QB00 max v(QB00) from=2469n to=2542n
if keep_12_QB00 > 2.5
 let failures = failures + 1
end
meas tran h_12_Q01 find v(Q01) at=2590n
if h_12_Q01 > 0.5
 let failures = failures + 1
end
meas tran keep_12_Q01 max v(Q01) from=2469n to=2542n
if keep_12_Q01 > 2.5
 let failures = failures + 1
end
meas tran h_12_QB01 find v(QB01) at=2590n
if h_12_QB01 < 4.5
 let failures = failures + 1
end
meas tran keep_12_QB01 min v(QB01) from=2469n to=2542n
if keep_12_QB01 < 2.5
 let failures = failures + 1
end
meas tran h_12_Q10 find v(Q10) at=2590n
if h_12_Q10 > 0.5
 let failures = failures + 1
end
meas tran keep_12_Q10 max v(Q10) from=2469n to=2542n
if keep_12_Q10 > 2.5
 let failures = failures + 1
end
meas tran h_12_QB10 find v(QB10) at=2590n
if h_12_QB10 < 4.5
 let failures = failures + 1
end
meas tran keep_12_QB10 min v(QB10) from=2469n to=2542n
if keep_12_QB10 < 2.5
 let failures = failures + 1
end
meas tran h_12_Q11 find v(Q11) at=2590n
if h_12_Q11 < 4.5
 let failures = failures + 1
end
meas tran keep_12_Q11 min v(Q11) from=2469n to=2542n
if keep_12_Q11 < 2.5
 let failures = failures + 1
end
meas tran h_12_QB11 find v(QB11) at=2590n
if h_12_QB11 > 0.5
 let failures = failures + 1
end
meas tran keep_12_QB11 max v(QB11) from=2469n to=2542n
if keep_12_QB11 > 2.5
 let failures = failures + 1
end
meas tran reset_12_SOUT find v(SOUT) at=2439n
if reset_12_SOUT < 4.5
 let failures = failures + 1
end
meas tran read_12_SOUT find v(SOUT) at=2550n
if read_12_SOUT < 4.5
 let failures = failures + 1
end
meas tran reset_12_SOUTB find v(SOUTB) at=2439n
if reset_12_SOUTB < 4.5
 let failures = failures + 1
end
meas tran read_12_SOUTB find v(SOUTB) at=2550n
if read_12_SOUTB > 0.5
 let failures = failures + 1
end
meas tran diff_12 find ydiff at=2490n
meas tran h_13_Q00 find v(Q00) at=2790n
if h_13_Q00 < 4.5
 let failures = failures + 1
end
meas tran keep_13_Q00 min v(Q00) from=2669n to=2742n
if keep_13_Q00 < 2.5
 let failures = failures + 1
end
meas tran h_13_QB00 find v(QB00) at=2790n
if h_13_QB00 > 0.5
 let failures = failures + 1
end
meas tran keep_13_QB00 max v(QB00) from=2669n to=2742n
if keep_13_QB00 > 2.5
 let failures = failures + 1
end
meas tran h_13_Q01 find v(Q01) at=2790n
if h_13_Q01 > 0.5
 let failures = failures + 1
end
meas tran keep_13_Q01 max v(Q01) from=2669n to=2742n
if keep_13_Q01 > 2.5
 let failures = failures + 1
end
meas tran h_13_QB01 find v(QB01) at=2790n
if h_13_QB01 < 4.5
 let failures = failures + 1
end
meas tran keep_13_QB01 min v(QB01) from=2669n to=2742n
if keep_13_QB01 < 2.5
 let failures = failures + 1
end
meas tran h_13_Q10 find v(Q10) at=2790n
if h_13_Q10 > 0.5
 let failures = failures + 1
end
meas tran keep_13_Q10 max v(Q10) from=2669n to=2742n
if keep_13_Q10 > 2.5
 let failures = failures + 1
end
meas tran h_13_QB10 find v(QB10) at=2790n
if h_13_QB10 < 4.5
 let failures = failures + 1
end
meas tran keep_13_QB10 min v(QB10) from=2669n to=2742n
if keep_13_QB10 < 2.5
 let failures = failures + 1
end
meas tran h_13_Q11 find v(Q11) at=2790n
if h_13_Q11 < 4.5
 let failures = failures + 1
end
meas tran keep_13_Q11 min v(Q11) from=2669n to=2742n
if keep_13_Q11 < 2.5
 let failures = failures + 1
end
meas tran h_13_QB11 find v(QB11) at=2790n
if h_13_QB11 > 0.5
 let failures = failures + 1
end
meas tran keep_13_QB11 max v(QB11) from=2669n to=2742n
if keep_13_QB11 > 2.5
 let failures = failures + 1
end
meas tran reset_13_SOUT find v(SOUT) at=2639n
if reset_13_SOUT < 4.5
 let failures = failures + 1
end
meas tran read_13_SOUT find v(SOUT) at=2750n
if read_13_SOUT > 0.5
 let failures = failures + 1
end
meas tran reset_13_SOUTB find v(SOUTB) at=2639n
if reset_13_SOUTB < 4.5
 let failures = failures + 1
end
meas tran read_13_SOUTB find v(SOUTB) at=2750n
if read_13_SOUTB < 4.5
 let failures = failures + 1
end
meas tran diff_13 find ydiff at=2690n
meas tran h_14_Q00 find v(Q00) at=2990n
if h_14_Q00 < 4.5
 let failures = failures + 1
end
meas tran keep_14_Q00 min v(Q00) from=2869n to=2942n
if keep_14_Q00 < 2.5
 let failures = failures + 1
end
meas tran h_14_QB00 find v(QB00) at=2990n
if h_14_QB00 > 0.5
 let failures = failures + 1
end
meas tran keep_14_QB00 max v(QB00) from=2869n to=2942n
if keep_14_QB00 > 2.5
 let failures = failures + 1
end
meas tran h_14_Q01 find v(Q01) at=2990n
if h_14_Q01 > 0.5
 let failures = failures + 1
end
meas tran keep_14_Q01 max v(Q01) from=2869n to=2942n
if keep_14_Q01 > 2.5
 let failures = failures + 1
end
meas tran h_14_QB01 find v(QB01) at=2990n
if h_14_QB01 < 4.5
 let failures = failures + 1
end
meas tran keep_14_QB01 min v(QB01) from=2869n to=2942n
if keep_14_QB01 < 2.5
 let failures = failures + 1
end
meas tran h_14_Q10 find v(Q10) at=2990n
if h_14_Q10 > 0.5
 let failures = failures + 1
end
meas tran keep_14_Q10 max v(Q10) from=2869n to=2942n
if keep_14_Q10 > 2.5
 let failures = failures + 1
end
meas tran h_14_QB10 find v(QB10) at=2990n
if h_14_QB10 < 4.5
 let failures = failures + 1
end
meas tran keep_14_QB10 min v(QB10) from=2869n to=2942n
if keep_14_QB10 < 2.5
 let failures = failures + 1
end
meas tran h_14_Q11 find v(Q11) at=2990n
if h_14_Q11 < 4.5
 let failures = failures + 1
end
meas tran keep_14_Q11 min v(Q11) from=2869n to=2942n
if keep_14_Q11 < 2.5
 let failures = failures + 1
end
meas tran h_14_QB11 find v(QB11) at=2990n
if h_14_QB11 > 0.5
 let failures = failures + 1
end
meas tran keep_14_QB11 max v(QB11) from=2869n to=2942n
if keep_14_QB11 > 2.5
 let failures = failures + 1
end
meas tran reset_14_SOUT find v(SOUT) at=2839n
if reset_14_SOUT < 4.5
 let failures = failures + 1
end
meas tran read_14_SOUT find v(SOUT) at=2950n
if read_14_SOUT > 0.5
 let failures = failures + 1
end
meas tran reset_14_SOUTB find v(SOUTB) at=2839n
if reset_14_SOUTB < 4.5
 let failures = failures + 1
end
meas tran read_14_SOUTB find v(SOUTB) at=2950n
if read_14_SOUTB < 4.5
 let failures = failures + 1
end
meas tran diff_14 find ydiff at=2890n
meas tran h_15_Q00 find v(Q00) at=3190n
if h_15_Q00 < 4.5
 let failures = failures + 1
end
meas tran keep_15_Q00 min v(Q00) from=3069n to=3142n
if keep_15_Q00 < 2.5
 let failures = failures + 1
end
meas tran h_15_QB00 find v(QB00) at=3190n
if h_15_QB00 > 0.5
 let failures = failures + 1
end
meas tran keep_15_QB00 max v(QB00) from=3069n to=3142n
if keep_15_QB00 > 2.5
 let failures = failures + 1
end
meas tran h_15_Q01 find v(Q01) at=3190n
if h_15_Q01 > 0.5
 let failures = failures + 1
end
meas tran keep_15_Q01 max v(Q01) from=3069n to=3142n
if keep_15_Q01 > 2.5
 let failures = failures + 1
end
meas tran h_15_QB01 find v(QB01) at=3190n
if h_15_QB01 < 4.5
 let failures = failures + 1
end
meas tran keep_15_QB01 min v(QB01) from=3069n to=3142n
if keep_15_QB01 < 2.5
 let failures = failures + 1
end
meas tran h_15_Q10 find v(Q10) at=3190n
if h_15_Q10 > 0.5
 let failures = failures + 1
end
meas tran keep_15_Q10 max v(Q10) from=3069n to=3142n
if keep_15_Q10 > 2.5
 let failures = failures + 1
end
meas tran h_15_QB10 find v(QB10) at=3190n
if h_15_QB10 < 4.5
 let failures = failures + 1
end
meas tran keep_15_QB10 min v(QB10) from=3069n to=3142n
if keep_15_QB10 < 2.5
 let failures = failures + 1
end
meas tran h_15_Q11 find v(Q11) at=3190n
if h_15_Q11 < 4.5
 let failures = failures + 1
end
meas tran keep_15_Q11 min v(Q11) from=3069n to=3142n
if keep_15_Q11 < 2.5
 let failures = failures + 1
end
meas tran h_15_QB11 find v(QB11) at=3190n
if h_15_QB11 > 0.5
 let failures = failures + 1
end
meas tran keep_15_QB11 max v(QB11) from=3069n to=3142n
if keep_15_QB11 > 2.5
 let failures = failures + 1
end
meas tran reset_15_SOUT find v(SOUT) at=3039n
if reset_15_SOUT < 4.5
 let failures = failures + 1
end
meas tran read_15_SOUT find v(SOUT) at=3150n
if read_15_SOUT < 4.5
 let failures = failures + 1
end
meas tran reset_15_SOUTB find v(SOUTB) at=3039n
if reset_15_SOUTB < 4.5
 let failures = failures + 1
end
meas tran read_15_SOUTB find v(SOUTB) at=3150n
if read_15_SOUTB > 0.5
 let failures = failures + 1
end
meas tran diff_15 find ydiff at=3090n
if failures = 0
 echo PASS: 2x2 mux writes, sensed reads, reset and unselected-cell retention
else
 echo FAIL: inspect measurements
 print failures
end
write sram_tb_array_mux.raw
plot v(Q00) v(Q01) v(Q10) v(Q11) title 'STORED BITS: checkerboard then inverse'
plot v(SOUT) v(SOUTB) title 'READ OUTPUTS: valid at cycle +150 ns'
plot v(BL0) v(BLB0) v(Y) v(YB) xlimit 840n 950n title 'READ row0 col0: local BL through NMOS mux to common Y'
plot v(Y) v(YB) v(SOUT) v(SOUTB) xlimit 840n 950n title 'READ row0 col0: SAE rises at 890 ns'
let PREB_T = v(PREB)/5+16
let YPREB_T = v(YPREB)/5+14
let COL0_T = v(COL0)/5+12
let COL1_T = v(COL1)/5+10
let WL0_T = v(WL0)/5+8
let WL1_T = v(WL1)/5+6
let SAE_T = v(SAE)/5+4
let PD_Y_T = v(PD_Y)/5+2
let PD_YB_T = v(PD_YB)/5+0
plot PREB_T YPREB_T WL0_T WL1_T COL0_T COL1_T PD_Y_T PD_YB_T SAE_T title 'CONTROLS: PREB16 YPREB14 COL0/1=12/10 WL0/1=8/6 SAE4 PD_Y/YB=2/0'
.endc

**** end user architecture code
**.ends
.GLOBAL GND
.end
